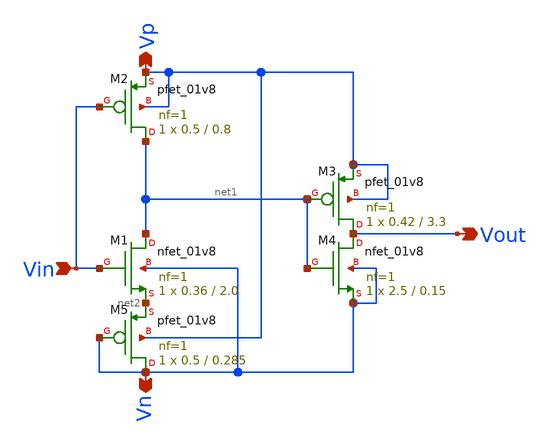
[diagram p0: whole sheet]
** sch_path: xschem/Vth_sch/Symbol/th15_1.sch
**.subckt th15_1 Vn Vp Vin Vout
*.opin Vn
*.opin Vp
*.ipin Vin
*.opin Vout
XM3 Vout net1 Vp Vp sky130_fd_pr__pfet_01v8 L=3.3 W=0.42 nf=1 ad='int((nf+1)/2) * W/nf * 0.29' as='int((nf+2)/2) * W/nf * 0.29'
+ pd='2*int((nf+1)/2) * (W/nf + 0.29)' ps='2*int((nf+2)/2) * (W/nf + 0.29)' nrd='0.29 / W' nrs='0.29 / W'
+ sa=0 sb=0 sd=0 mult=1 m=1
XM4 Vout net1 Vn Vn sky130_fd_pr__nfet_01v8 L=0.15 W=2.5 nf=1 ad='int((nf+1)/2) * W/nf * 0.29' as='int((nf+2)/2) * W/nf * 0.29'
+ pd='2*int((nf+1)/2) * (W/nf + 0.29)' ps='2*int((nf+2)/2) * (W/nf + 0.29)' nrd='0.29 / W' nrs='0.29 / W'
+ sa=0 sb=0 sd=0 mult=1 m=1
XM2 net1 Vin Vp Vp sky130_fd_pr__pfet_01v8 L=0.8 W=0.5 nf=1 ad='int((nf+1)/2) * W/nf * 0.29' as='int((nf+2)/2) * W/nf * 0.29'
+ pd='2*int((nf+1)/2) * (W/nf + 0.29)' ps='2*int((nf+2)/2) * (W/nf + 0.29)' nrd='0.29 / W' nrs='0.29 / W'
+ sa=0 sb=0 sd=0 mult=1 m=1
XM1 net1 Vin net2 Vn sky130_fd_pr__nfet_01v8 L=2.0 W=0.36 nf=1 ad='int((nf+1)/2) * W/nf * 0.29' as='int((nf+2)/2) * W/nf * 0.29'
+ pd='2*int((nf+1)/2) * (W/nf + 0.29)' ps='2*int((nf+2)/2) * (W/nf + 0.29)' nrd='0.29 / W' nrs='0.29 / W'
+ sa=0 sb=0 sd=0 mult=1 m=1
XM5 Vn Vn net2 Vp sky130_fd_pr__pfet_01v8 L=0.285 W=0.5 nf=1 ad='int((nf+1)/2) * W/nf * 0.29' as='int((nf+2)/2) * W/nf * 0.29'
+ pd='2*int((nf+1)/2) * (W/nf + 0.29)' ps='2*int((nf+2)/2) * (W/nf + 0.29)' nrd='0.29 / W' nrs='0.29 / W'
+ sa=0 sb=0 sd=0 mult=1 m=1
**.ends
.end
